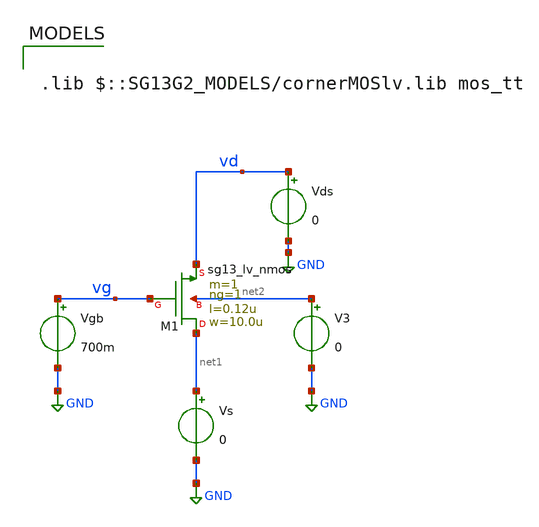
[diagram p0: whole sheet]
** sch_path: ihp_tutorials/nmos_idvd.sch
**.subckt nmos_idvd
Vds vd GND 0
V3 net2 GND 0
Vs net1 GND 0
Vgb vg GND 700m
XM1 net1 vg vd net2 sg13_lv_nmos w=10.0u l=0.12u ng=1 m=1 mm_ok=1
**** begin user architecture code



.control
pre_osdi ./psp103_nqs.osdi
save all

dc Vds 0.001 1.5 1m

let gmd = deriv(i(Vs))
save gmd

write nmos_idvd.raw

.endc




.lib $::SG13G2_MODELS/cornerMOSlv.lib mos_tt

**** end user architecture code
**.ends
.GLOBAL GND
.end
